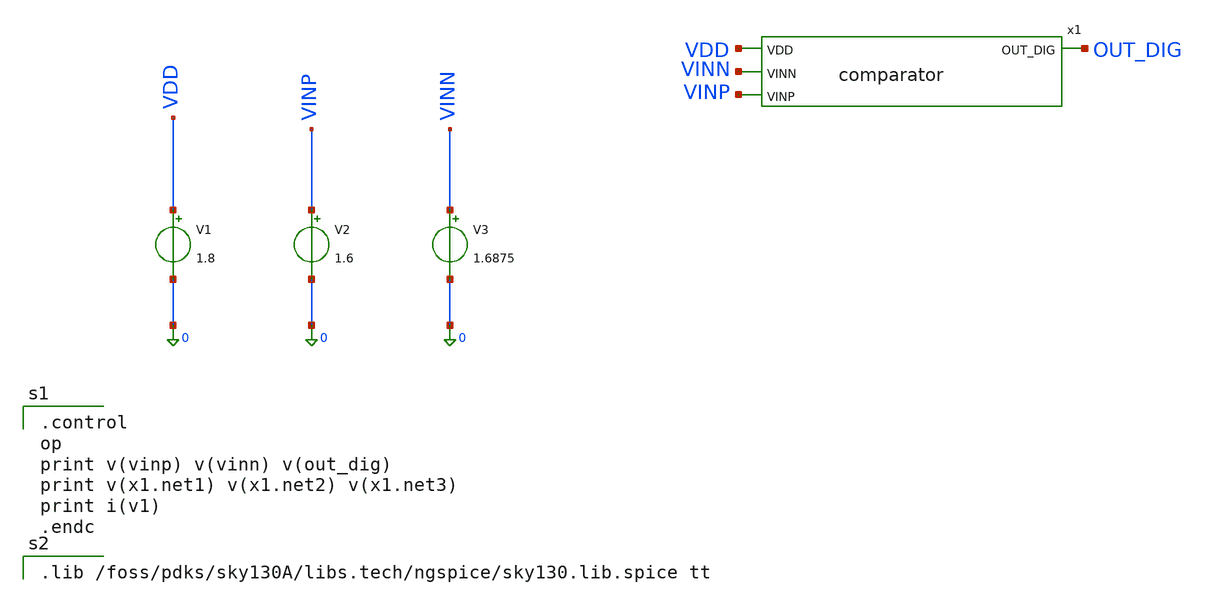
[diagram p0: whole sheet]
** sch_path: comparator_tb.sch
**.subckt comparator_tb
V1 VDD 0 1.8
V2 VINP 0 1.6
V3 VINN 0 1.6875
x1 VDD OUT_DIG VINN VINP comparator
**** begin user architecture code

.control
op
print v(vinp) v(vinn) v(out_dig)
print v(x1.net1) v(x1.net2) v(x1.net3)
print i(v1)
.endc


.lib /foss/pdks/sky130A/libs.tech/ngspice/sky130.lib.spice tt

**** end user architecture code
**.ends

* expanding   symbol:  comparator.sym # of pins=4
** sym_path: comparator.sym
** sch_path: comparator.sch
.subckt comparator VDD OUT_DIG VINN VINP
*.ipin VINP
*.ipin VINN
*.ipin VDD
*.opin OUT_DIG
I0 net1 0 20uA
XM1 net2 VINP net1 0 sky130_fd_pr__nfet_01v8 L=0.15 W=1 nf=1 ad='int((1 + 1)/2) * 1 / 1 * 0.29' as='int((1 + 2)/2) * 1 / 1 * 0.29'
+ pd='2*int((1 + 1)/2) * (1 / 1 + 0.29)' ps='2*int((1 + 2)/2) * (1 / 1 + 0.29)' nrd='0.29 / 1 ' nrs='0.29 / 1 '
+ sa=0 sb=0 sd=0 mult=1 m=1
XM2 net3 VINN net1 0 sky130_fd_pr__nfet_01v8 L=0.15 W=1 nf=1 ad='int((1 + 1)/2) * 1 / 1 * 0.29' as='int((1 + 2)/2) * 1 / 1 * 0.29'
+ pd='2*int((1 + 1)/2) * (1 / 1 + 0.29)' ps='2*int((1 + 2)/2) * (1 / 1 + 0.29)' nrd='0.29 / 1 ' nrs='0.29 / 1 '
+ sa=0 sb=0 sd=0 mult=1 m=1
XM6 OUT_DIG net3 0 0 sky130_fd_pr__nfet_01v8 L=0.15 W=1 nf=1 ad='int((1 + 1)/2) * 1 / 1 * 0.29' as='int((1 + 2)/2) * 1 / 1 * 0.29'
+ pd='2*int((1 + 1)/2) * (1 / 1 + 0.29)' ps='2*int((1 + 2)/2) * (1 / 1 + 0.29)' nrd='0.29 / 1 ' nrs='0.29 / 1 '
+ sa=0 sb=0 sd=0 mult=1 m=1
XM3 net2 net2 VDD VDD sky130_fd_pr__pfet_01v8 L=0.15 W=1 nf=1 ad='int((1 + 1)/2) * 1 / 1 * 0.29' as='int((1 + 2)/2) * 1 / 1 * 0.29'
+ pd='2*int((1 + 1)/2) * (1 / 1 + 0.29)' ps='2*int((1 + 2)/2) * (1 / 1 + 0.29)' nrd='0.29 / 1 ' nrs='0.29 / 1 '
+ sa=0 sb=0 sd=0 mult=1 m=1
XM4 net3 net2 VDD VDD sky130_fd_pr__pfet_01v8 L=0.15 W=1 nf=1 ad='int((1 + 1)/2) * 1 / 1 * 0.29' as='int((1 + 2)/2) * 1 / 1 * 0.29'
+ pd='2*int((1 + 1)/2) * (1 / 1 + 0.29)' ps='2*int((1 + 2)/2) * (1 / 1 + 0.29)' nrd='0.29 / 1 ' nrs='0.29 / 1 '
+ sa=0 sb=0 sd=0 mult=1 m=1
XM5 OUT_DIG net3 VDD VDD sky130_fd_pr__pfet_01v8 L=0.15 W=1 nf=1 ad='int((1 + 1)/2) * 1 / 1 * 0.29' as='int((1 + 2)/2) * 1 / 1 * 0.29'
+ pd='2*int((1 + 1)/2) * (1 / 1 + 0.29)' ps='2*int((1 + 2)/2) * (1 / 1 + 0.29)' nrd='0.29 / 1 ' nrs='0.29 / 1 '
+ sa=0 sb=0 sd=0 mult=1 m=1
.ends

.end
